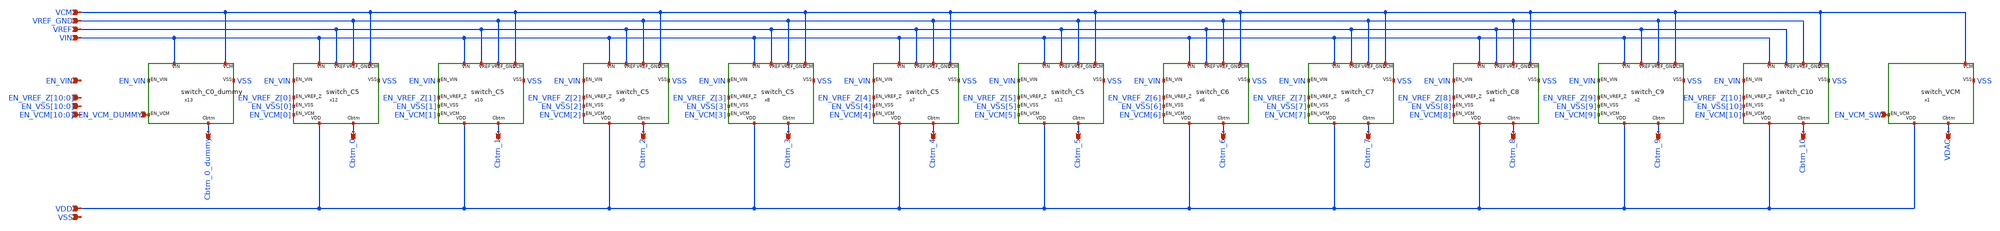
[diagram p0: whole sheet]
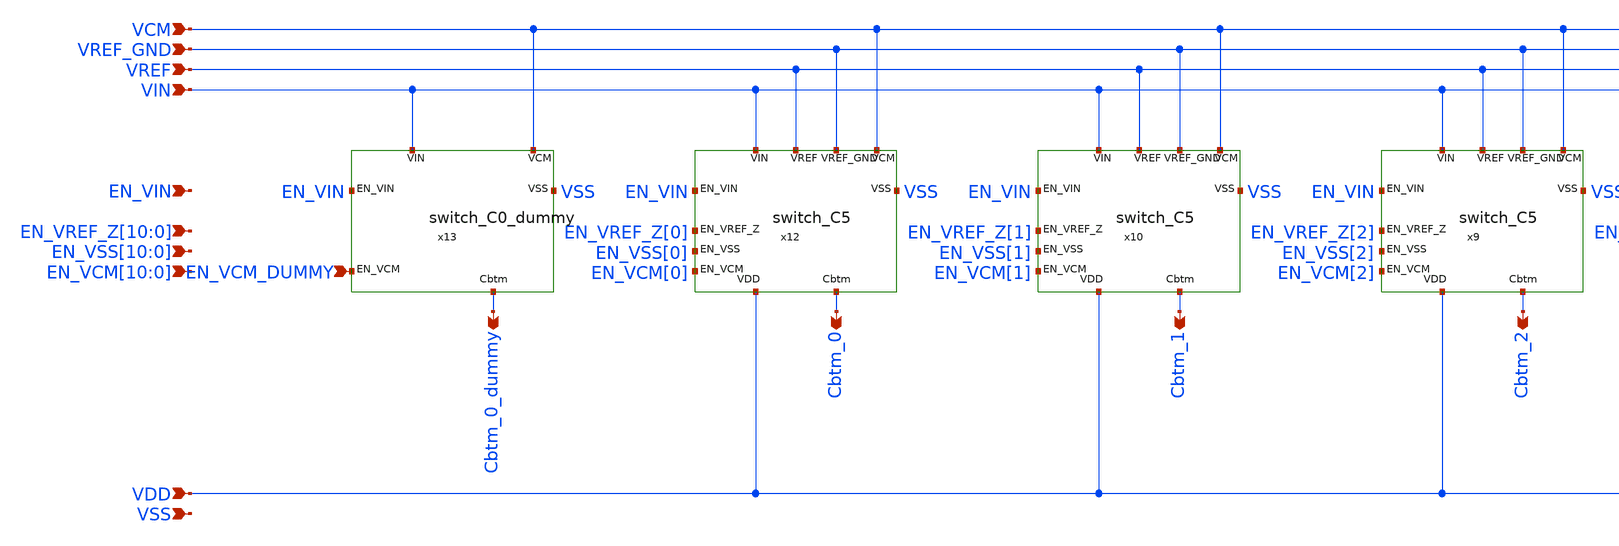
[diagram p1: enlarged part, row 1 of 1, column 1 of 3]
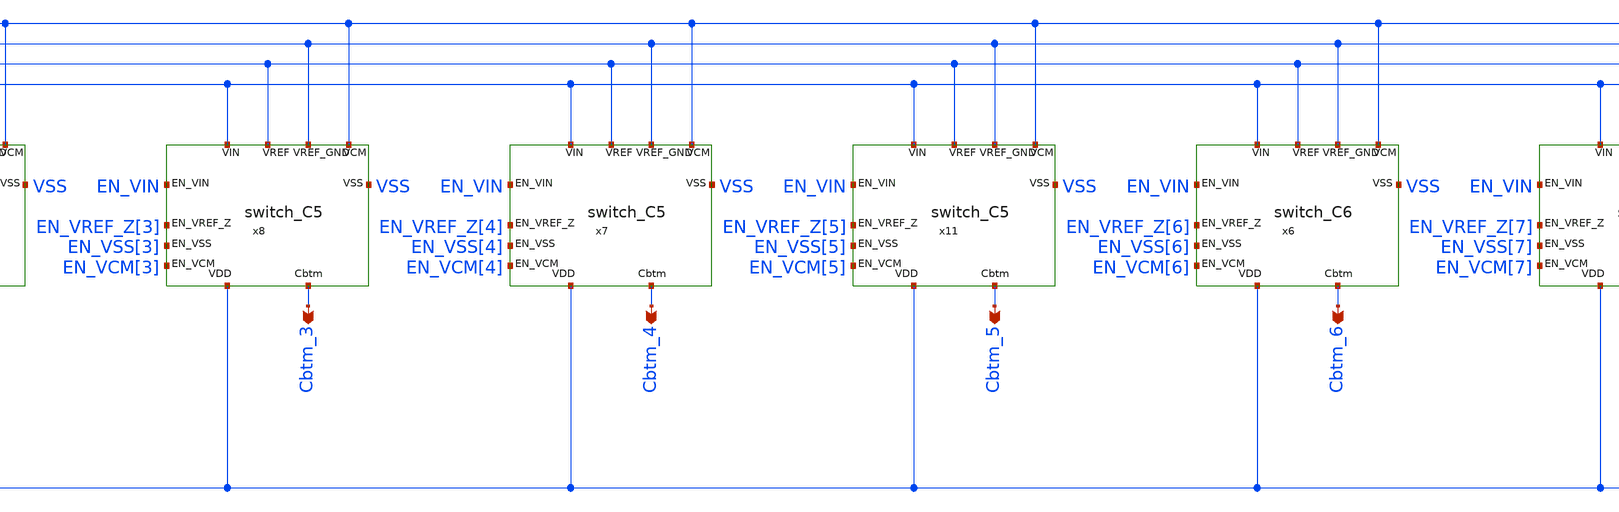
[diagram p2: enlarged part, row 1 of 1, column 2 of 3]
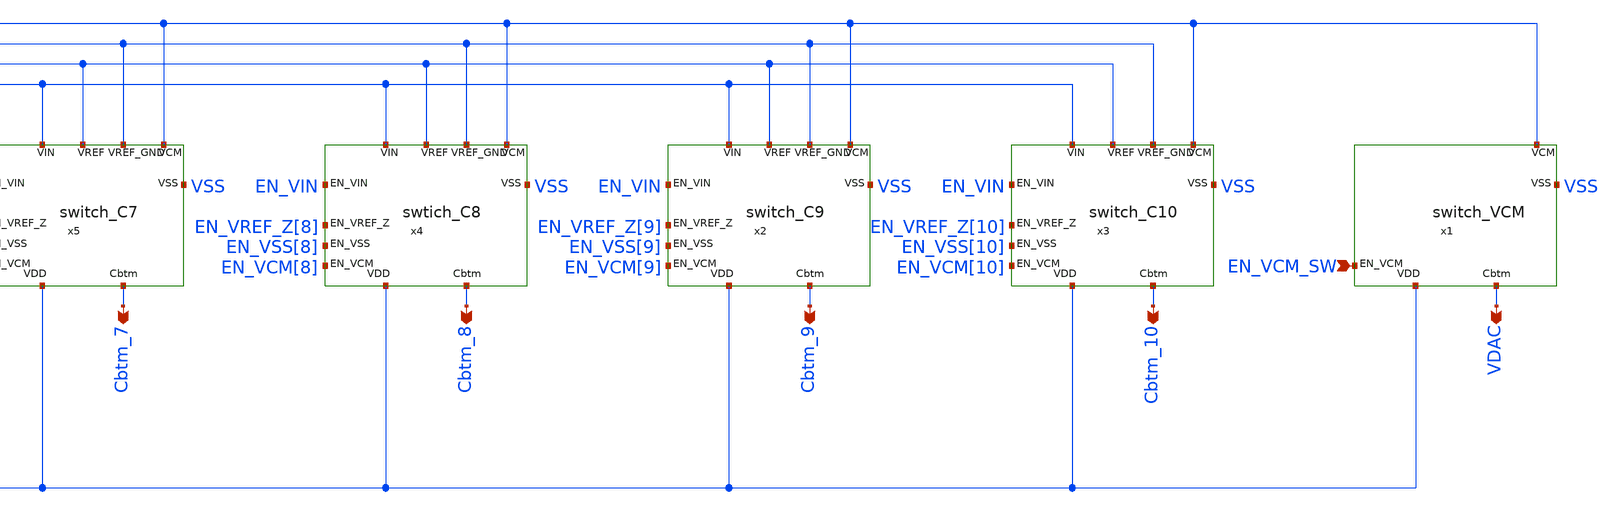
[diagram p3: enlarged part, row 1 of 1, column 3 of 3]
** sch_path: Schematic/switches/switches.sch
**.subckt switches VCM VREF_GND VREF VIN VDD Cbtm_0_dummy Cbtm_0 Cbtm_1 Cbtm_2 Cbtm_3 Cbtm_4 Cbtm_5
*+ Cbtm_6 Cbtm_7 Cbtm_8 Cbtm_9 Cbtm_10 VDAC EN_VIN
*+ EN_VREF_Z[10],EN_VREF_Z[9],EN_VREF_Z[8],EN_VREF_Z[7],EN_VREF_Z[6],EN_VREF_Z[5],EN_VREF_Z[4],EN_VREF_Z[3],EN_VREF_Z[2],EN_VREF_Z[1],EN_VREF_Z[0]
*+ EN_VSS[10],EN_VSS[9],EN_VSS[8],EN_VSS[7],EN_VSS[6],EN_VSS[5],EN_VSS[4],EN_VSS[3],EN_VSS[2],EN_VSS[1],EN_VSS[0]
*+ EN_VCM[10],EN_VCM[9],EN_VCM[8],EN_VCM[7],EN_VCM[6],EN_VCM[5],EN_VCM[4],EN_VCM[3],EN_VCM[2],EN_VCM[1],EN_VCM[0] EN_VCM_DUMMY EN_VCM_SW VSS
*.ipin VCM
*.ipin VREF_GND
*.ipin VREF
*.ipin VIN
*.ipin VDD
*.opin Cbtm_0_dummy
*.opin Cbtm_0
*.opin Cbtm_1
*.opin Cbtm_2
*.opin Cbtm_3
*.opin Cbtm_4
*.opin Cbtm_5
*.opin Cbtm_6
*.opin Cbtm_7
*.opin Cbtm_8
*.opin Cbtm_9
*.opin Cbtm_10
*.opin VDAC
*.ipin EN_VIN
*.ipin
*+ EN_VREF_Z[10],EN_VREF_Z[9],EN_VREF_Z[8],EN_VREF_Z[7],EN_VREF_Z[6],EN_VREF_Z[5],EN_VREF_Z[4],EN_VREF_Z[3],EN_VREF_Z[2],EN_VREF_Z[1],EN_VREF_Z[0]
*.ipin
*+ EN_VSS[10],EN_VSS[9],EN_VSS[8],EN_VSS[7],EN_VSS[6],EN_VSS[5],EN_VSS[4],EN_VSS[3],EN_VSS[2],EN_VSS[1],EN_VSS[0]
*.ipin
*+ EN_VCM[10],EN_VCM[9],EN_VCM[8],EN_VCM[7],EN_VCM[6],EN_VCM[5],EN_VCM[4],EN_VCM[3],EN_VCM[2],EN_VCM[1],EN_VCM[0]
*.ipin EN_VCM_DUMMY
*.ipin EN_VCM_SW
*.ipin VSS
x1 VCM EN_VCM_SW VDAC VDD VSS switch_VCM
x3 VCM VREF_GND VIN VREF EN_VCM[10] EN_VREF_Z[10] Cbtm_10 VDD EN_VSS[10] EN_VIN VSS switch_C10
x2 VCM VREF_GND VIN VREF EN_VCM[9] EN_VREF_Z[9] Cbtm_9 VDD EN_VSS[9] EN_VIN VSS switch_C9
x4 VCM VREF_GND VIN VREF EN_VCM[8] EN_VREF_Z[8] Cbtm_8 VDD EN_VSS[8] EN_VIN VSS swtich_C8
x5 VCM VREF_GND VIN VREF EN_VCM[7] EN_VREF_Z[7] Cbtm_7 VDD EN_VSS[7] EN_VIN VSS switch_C7
x6 VCM VREF_GND VIN VREF EN_VCM[6] EN_VREF_Z[6] Cbtm_6 VDD EN_VSS[6] EN_VIN VSS switch_C6
x11 VCM VREF_GND VIN VREF EN_VCM[5] EN_VREF_Z[5] Cbtm_5 VDD EN_VSS[5] EN_VIN VSS switch_C5
x7 VCM VREF_GND VIN VREF EN_VCM[4] EN_VREF_Z[4] Cbtm_4 VDD EN_VSS[4] EN_VIN VSS switch_C5
x8 VCM VREF_GND VIN VREF EN_VCM[3] EN_VREF_Z[3] Cbtm_3 VDD EN_VSS[3] EN_VIN VSS switch_C5
x9 VCM VREF_GND VIN VREF EN_VCM[2] EN_VREF_Z[2] Cbtm_2 VDD EN_VSS[2] EN_VIN VSS switch_C5
x10 VCM VREF_GND VIN VREF EN_VCM[1] EN_VREF_Z[1] Cbtm_1 VDD EN_VSS[1] EN_VIN VSS switch_C5
x12 VCM VREF_GND VIN VREF EN_VCM[0] EN_VREF_Z[0] Cbtm_0 VDD EN_VSS[0] EN_VIN VSS switch_C5
x13 VCM VIN EN_VCM_DUMMY Cbtm_0_dummy EN_VIN VSS switch_C0_dummy
**.ends

* expanding   symbol:  individual_switch/switch_VCM.sym # of pins=5
** sym_path: Schematic/individual_switch/switch_VCM.sym
** sch_path: Schematic/individual_switch/switch_VCM.sch
.subckt switch_VCM VCM EN_VCM Cbtm VDD VSS
*.ipin VCM
*.ipin EN_VCM
*.opin Cbtm
*.ipin VSS
*.ipin VDD
XM1 VCM EN_VCM Cbtm VSS nfet_03v3 L=0.28u W=128u nf=16 ad='int((nf+1)/2) * W/nf * 0.18u' as='int((nf+2)/2) * W/nf * 0.18u'
+ pd='2*int((nf+1)/2) * (W/nf + 0.18u)' ps='2*int((nf+2)/2) * (W/nf + 0.18u)' nrd='0.18u / W' nrs='0.18u / W'
+ sa=0 sb=0 sd=0 m=1
.ends


* expanding   symbol:  individual_switch/switch_C10.sym # of pins=11
** sym_path: Schematic/individual_switch/switch_C10.sym
** sch_path: Schematic/individual_switch/switch_C10.sch
.subckt switch_C10 VCM VREF_GND VIN VREF EN_VCM EN_VREF_Z Cbtm VDD EN_VSS EN_VIN VSS
*.ipin VIN
*.ipin EN_VIN
*.ipin VREF_GND
*.ipin VREF
*.ipin VCM
*.ipin EN_VCM
*.opin Cbtm
*.ipin VDD
*.ipin EN_VSS
*.ipin EN_VREF_Z
*.ipin VSS
XM1 VIN EN_VIN Cbtm VSS nfet_03v3 L=0.28u W=32u nf=4 ad='int((nf+1)/2) * W/nf * 0.18u' as='int((nf+2)/2) * W/nf * 0.18u'
+ pd='2*int((nf+1)/2) * (W/nf + 0.18u)' ps='2*int((nf+2)/2) * (W/nf + 0.18u)' nrd='0.18u / W' nrs='0.18u / W'
+ sa=0 sb=0 sd=0 m=1
XM2 VREF_GND EN_VSS Cbtm VSS nfet_03v3 L=0.28u W=128u nf=16 ad='int((nf+1)/2) * W/nf * 0.18u' as='int((nf+2)/2) * W/nf * 0.18u'
+ pd='2*int((nf+1)/2) * (W/nf + 0.18u)' ps='2*int((nf+2)/2) * (W/nf + 0.18u)' nrd='0.18u / W' nrs='0.18u / W'
+ sa=0 sb=0 sd=0 m=1
XM3 VCM EN_VCM Cbtm VSS nfet_03v3 L=0.28u W=128u nf=16 ad='int((nf+1)/2) * W/nf * 0.18u' as='int((nf+2)/2) * W/nf * 0.18u'
+ pd='2*int((nf+1)/2) * (W/nf + 0.18u)' ps='2*int((nf+2)/2) * (W/nf + 0.18u)' nrd='0.18u / W' nrs='0.18u / W'
+ sa=0 sb=0 sd=0 m=1
XM4 Cbtm EN_VREF_Z VREF VDD pfet_03v3 L=0.28u W=256u nf=32 ad='int((nf+1)/2) * W/nf * 0.18u' as='int((nf+2)/2) * W/nf * 0.18u'
+ pd='2*int((nf+1)/2) * (W/nf + 0.18u)' ps='2*int((nf+2)/2) * (W/nf + 0.18u)' nrd='0.18u / W' nrs='0.18u / W'
+ sa=0 sb=0 sd=0 m=1
.ends


* expanding   symbol:  individual_switch/switch_C9.sym # of pins=11
** sym_path: Schematic/individual_switch/switch_C9.sym
** sch_path: Schematic/individual_switch/switch_C9.sch
.subckt switch_C9 VCM VREF_GND VIN VREF EN_VCM EN_VREF_Z Cbtm VDD EN_VSS EN_VIN VSS
*.ipin VIN
*.ipin EN_VIN
*.ipin VREF_GND
*.ipin VREF
*.ipin VCM
*.ipin EN_VCM
*.opin Cbtm
*.ipin VDD
*.ipin EN_VSS
*.ipin EN_VREF_Z
*.ipin VSS
XM1 VIN EN_VIN Cbtm VSS nfet_03v3 L=0.28u W=16u nf=2 ad='int((nf+1)/2) * W/nf * 0.18u' as='int((nf+2)/2) * W/nf * 0.18u'
+ pd='2*int((nf+1)/2) * (W/nf + 0.18u)' ps='2*int((nf+2)/2) * (W/nf + 0.18u)' nrd='0.18u / W' nrs='0.18u / W'
+ sa=0 sb=0 sd=0 m=1
XM2 VREF_GND EN_VSS Cbtm VSS nfet_03v3 L=0.28u W=64u nf=8 ad='int((nf+1)/2) * W/nf * 0.18u' as='int((nf+2)/2) * W/nf * 0.18u'
+ pd='2*int((nf+1)/2) * (W/nf + 0.18u)' ps='2*int((nf+2)/2) * (W/nf + 0.18u)' nrd='0.18u / W' nrs='0.18u / W'
+ sa=0 sb=0 sd=0 m=1
XM3 VCM EN_VCM Cbtm VSS nfet_03v3 L=0.28u W=64u nf=8 ad='int((nf+1)/2) * W/nf * 0.18u' as='int((nf+2)/2) * W/nf * 0.18u'
+ pd='2*int((nf+1)/2) * (W/nf + 0.18u)' ps='2*int((nf+2)/2) * (W/nf + 0.18u)' nrd='0.18u / W' nrs='0.18u / W'
+ sa=0 sb=0 sd=0 m=1
XM4 Cbtm EN_VREF_Z VREF VDD pfet_03v3 L=0.28u W=128u nf=16 ad='int((nf+1)/2) * W/nf * 0.18u' as='int((nf+2)/2) * W/nf * 0.18u'
+ pd='2*int((nf+1)/2) * (W/nf + 0.18u)' ps='2*int((nf+2)/2) * (W/nf + 0.18u)' nrd='0.18u / W' nrs='0.18u / W'
+ sa=0 sb=0 sd=0 m=1
.ends


* expanding   symbol:  individual_switch/swtich_C8.sym # of pins=11
** sym_path: Schematic/individual_switch/swtich_C8.sym
** sch_path: Schematic/individual_switch/swtich_C8.sch
.subckt swtich_C8 VCM VREF_GND VIN VREF EN_VCM EN_VREF_Z Cbtm VDD EN_VSS EN_VIN VSS
*.ipin VIN
*.ipin EN_VIN
*.ipin VREF_GND
*.ipin VREF
*.ipin VCM
*.ipin EN_VCM
*.opin Cbtm
*.ipin VDD
*.ipin EN_VSS
*.ipin EN_VREF_Z
*.ipin VSS
XM1 VIN EN_VIN Cbtm VSS nfet_03v3 L=0.28u W=8u nf=1 ad='int((nf+1)/2) * W/nf * 0.18u' as='int((nf+2)/2) * W/nf * 0.18u'
+ pd='2*int((nf+1)/2) * (W/nf + 0.18u)' ps='2*int((nf+2)/2) * (W/nf + 0.18u)' nrd='0.18u / W' nrs='0.18u / W'
+ sa=0 sb=0 sd=0 m=1
XM2 VREF_GND EN_VSS Cbtm VSS nfet_03v3 L=0.28u W=32u nf=4 ad='int((nf+1)/2) * W/nf * 0.18u' as='int((nf+2)/2) * W/nf * 0.18u'
+ pd='2*int((nf+1)/2) * (W/nf + 0.18u)' ps='2*int((nf+2)/2) * (W/nf + 0.18u)' nrd='0.18u / W' nrs='0.18u / W'
+ sa=0 sb=0 sd=0 m=1
XM3 VCM EN_VCM Cbtm VSS nfet_03v3 L=0.28u W=32u nf=4 ad='int((nf+1)/2) * W/nf * 0.18u' as='int((nf+2)/2) * W/nf * 0.18u'
+ pd='2*int((nf+1)/2) * (W/nf + 0.18u)' ps='2*int((nf+2)/2) * (W/nf + 0.18u)' nrd='0.18u / W' nrs='0.18u / W'
+ sa=0 sb=0 sd=0 m=1
XM4 Cbtm EN_VREF_Z VREF VDD pfet_03v3 L=0.28u W=64u nf=8 ad='int((nf+1)/2) * W/nf * 0.18u' as='int((nf+2)/2) * W/nf * 0.18u'
+ pd='2*int((nf+1)/2) * (W/nf + 0.18u)' ps='2*int((nf+2)/2) * (W/nf + 0.18u)' nrd='0.18u / W' nrs='0.18u / W'
+ sa=0 sb=0 sd=0 m=1
.ends


* expanding   symbol:  individual_switch/switch_C7.sym # of pins=11
** sym_path: Schematic/individual_switch/switch_C7.sym
** sch_path: Schematic/individual_switch/switch_C7.sch
.subckt switch_C7 VCM VREF_GND VIN VREF EN_VCM EN_VREF_Z Cbtm VDD EN_VSS EN_VIN VSS
*.ipin VIN
*.ipin EN_VIN
*.ipin VREF_GND
*.ipin VREF
*.ipin VCM
*.ipin EN_VCM
*.opin Cbtm
*.ipin VDD
*.ipin EN_VSS
*.ipin EN_VREF_Z
*.ipin VSS
XM1 VIN EN_VIN Cbtm VSS nfet_03v3 L=0.28u W=4u nf=1 ad='int((nf+1)/2) * W/nf * 0.18u' as='int((nf+2)/2) * W/nf * 0.18u'
+ pd='2*int((nf+1)/2) * (W/nf + 0.18u)' ps='2*int((nf+2)/2) * (W/nf + 0.18u)' nrd='0.18u / W' nrs='0.18u / W'
+ sa=0 sb=0 sd=0 m=1
XM2 VREF_GND EN_VSS Cbtm VSS nfet_03v3 L=0.28u W=16u nf=2 ad='int((nf+1)/2) * W/nf * 0.18u' as='int((nf+2)/2) * W/nf * 0.18u'
+ pd='2*int((nf+1)/2) * (W/nf + 0.18u)' ps='2*int((nf+2)/2) * (W/nf + 0.18u)' nrd='0.18u / W' nrs='0.18u / W'
+ sa=0 sb=0 sd=0 m=1
XM3 VCM EN_VCM Cbtm VSS nfet_03v3 L=0.28u W=16u nf=2 ad='int((nf+1)/2) * W/nf * 0.18u' as='int((nf+2)/2) * W/nf * 0.18u'
+ pd='2*int((nf+1)/2) * (W/nf + 0.18u)' ps='2*int((nf+2)/2) * (W/nf + 0.18u)' nrd='0.18u / W' nrs='0.18u / W'
+ sa=0 sb=0 sd=0 m=1
XM4 Cbtm EN_VREF_Z VREF VDD pfet_03v3 L=0.28u W=32u nf=4 ad='int((nf+1)/2) * W/nf * 0.18u' as='int((nf+2)/2) * W/nf * 0.18u'
+ pd='2*int((nf+1)/2) * (W/nf + 0.18u)' ps='2*int((nf+2)/2) * (W/nf + 0.18u)' nrd='0.18u / W' nrs='0.18u / W'
+ sa=0 sb=0 sd=0 m=1
.ends


* expanding   symbol:  individual_switch/switch_C6.sym # of pins=11
** sym_path: Schematic/individual_switch/switch_C6.sym
** sch_path: Schematic/individual_switch/switch_C6.sch
.subckt switch_C6 VCM VREF_GND VIN VREF EN_VCM EN_VREF_Z Cbtm VDD EN_VSS EN_VIN VSS
*.ipin VIN
*.ipin EN_VIN
*.ipin VREF_GND
*.ipin VREF
*.ipin VCM
*.ipin EN_VCM
*.opin Cbtm
*.ipin VDD
*.ipin EN_VSS
*.ipin EN_VREF_Z
*.ipin VSS
XM1 VIN EN_VIN Cbtm VSS nfet_03v3 L=0.28u W=2u nf=1 ad='int((nf+1)/2) * W/nf * 0.18u' as='int((nf+2)/2) * W/nf * 0.18u'
+ pd='2*int((nf+1)/2) * (W/nf + 0.18u)' ps='2*int((nf+2)/2) * (W/nf + 0.18u)' nrd='0.18u / W' nrs='0.18u / W'
+ sa=0 sb=0 sd=0 m=1
XM2 VREF_GND EN_VSS Cbtm VSS nfet_03v3 L=0.28u W=8u nf=1 ad='int((nf+1)/2) * W/nf * 0.18u' as='int((nf+2)/2) * W/nf * 0.18u'
+ pd='2*int((nf+1)/2) * (W/nf + 0.18u)' ps='2*int((nf+2)/2) * (W/nf + 0.18u)' nrd='0.18u / W' nrs='0.18u / W'
+ sa=0 sb=0 sd=0 m=1
XM3 VCM EN_VCM Cbtm VSS nfet_03v3 L=0.28u W=8u nf=1 ad='int((nf+1)/2) * W/nf * 0.18u' as='int((nf+2)/2) * W/nf * 0.18u'
+ pd='2*int((nf+1)/2) * (W/nf + 0.18u)' ps='2*int((nf+2)/2) * (W/nf + 0.18u)' nrd='0.18u / W' nrs='0.18u / W'
+ sa=0 sb=0 sd=0 m=1
XM4 Cbtm EN_VREF_Z VREF VDD pfet_03v3 L=0.28u W=16u nf=1 ad='int((nf+1)/2) * W/nf * 0.18u' as='int((nf+2)/2) * W/nf * 0.18u'
+ pd='2*int((nf+1)/2) * (W/nf + 0.18u)' ps='2*int((nf+2)/2) * (W/nf + 0.18u)' nrd='0.18u / W' nrs='0.18u / W'
+ sa=0 sb=0 sd=0 m=1
.ends


* expanding   symbol:  individual_switch/switch_C5.sym # of pins=11
** sym_path: Schematic/individual_switch/switch_C5.sym
** sch_path: Schematic/individual_switch/switch_C5.sch
.subckt switch_C5 VCM VREF_GND VIN VREF EN_VCM EN_VREF_Z Cbtm VDD EN_VSS EN_VIN VSS
*.ipin VIN
*.ipin EN_VIN
*.ipin VREF_GND
*.ipin VREF
*.ipin VCM
*.ipin EN_VCM
*.opin Cbtm
*.ipin VDD
*.ipin EN_VSS
*.ipin EN_VREF_Z
*.ipin VSS
XM1 VIN EN_VIN Cbtm VSS nfet_03v3 L=0.28u W=2u nf=1 ad='int((nf+1)/2) * W/nf * 0.18u' as='int((nf+2)/2) * W/nf * 0.18u'
+ pd='2*int((nf+1)/2) * (W/nf + 0.18u)' ps='2*int((nf+2)/2) * (W/nf + 0.18u)' nrd='0.18u / W' nrs='0.18u / W'
+ sa=0 sb=0 sd=0 m=1
XM2 VREF_GND EN_VSS Cbtm VSS nfet_03v3 L=0.28u W=4u nf=1 ad='int((nf+1)/2) * W/nf * 0.18u' as='int((nf+2)/2) * W/nf * 0.18u'
+ pd='2*int((nf+1)/2) * (W/nf + 0.18u)' ps='2*int((nf+2)/2) * (W/nf + 0.18u)' nrd='0.18u / W' nrs='0.18u / W'
+ sa=0 sb=0 sd=0 m=1
XM3 VCM EN_VCM Cbtm VSS nfet_03v3 L=0.28u W=4u nf=1 ad='int((nf+1)/2) * W/nf * 0.18u' as='int((nf+2)/2) * W/nf * 0.18u'
+ pd='2*int((nf+1)/2) * (W/nf + 0.18u)' ps='2*int((nf+2)/2) * (W/nf + 0.18u)' nrd='0.18u / W' nrs='0.18u / W'
+ sa=0 sb=0 sd=0 m=1
XM4 Cbtm EN_VREF_Z VREF VDD pfet_03v3 L=0.28u W=8u nf=1 ad='int((nf+1)/2) * W/nf * 0.18u' as='int((nf+2)/2) * W/nf * 0.18u'
+ pd='2*int((nf+1)/2) * (W/nf + 0.18u)' ps='2*int((nf+2)/2) * (W/nf + 0.18u)' nrd='0.18u / W' nrs='0.18u / W'
+ sa=0 sb=0 sd=0 m=1
.ends


* expanding   symbol:  individual_switch/switch_C0_dummy.sym # of pins=6
** sym_path: Schematic/individual_switch/switch_C0_dummy.sym
** sch_path: Schematic/individual_switch/switch_C0_dummy.sch
.subckt switch_C0_dummy VCM VIN EN_VCM Cbtm EN_VIN VSS
*.ipin VIN
*.ipin EN_VIN
*.ipin VCM
*.ipin EN_VCM
*.opin Cbtm
*.ipin VSS
XM1 VIN EN_VIN Cbtm VSS nfet_03v3 L=0.28u W=2u nf=1 ad='int((nf+1)/2) * W/nf * 0.18u' as='int((nf+2)/2) * W/nf * 0.18u'
+ pd='2*int((nf+1)/2) * (W/nf + 0.18u)' ps='2*int((nf+2)/2) * (W/nf + 0.18u)' nrd='0.18u / W' nrs='0.18u / W'
+ sa=0 sb=0 sd=0 m=1
XM2 VCM EN_VCM Cbtm VSS nfet_03v3 L=0.28u W=3u nf=1 ad='int((nf+1)/2) * W/nf * 0.18u' as='int((nf+2)/2) * W/nf * 0.18u'
+ pd='2*int((nf+1)/2) * (W/nf + 0.18u)' ps='2*int((nf+2)/2) * (W/nf + 0.18u)' nrd='0.18u / W' nrs='0.18u / W'
+ sa=0 sb=0 sd=0 m=1
.ends

.end
